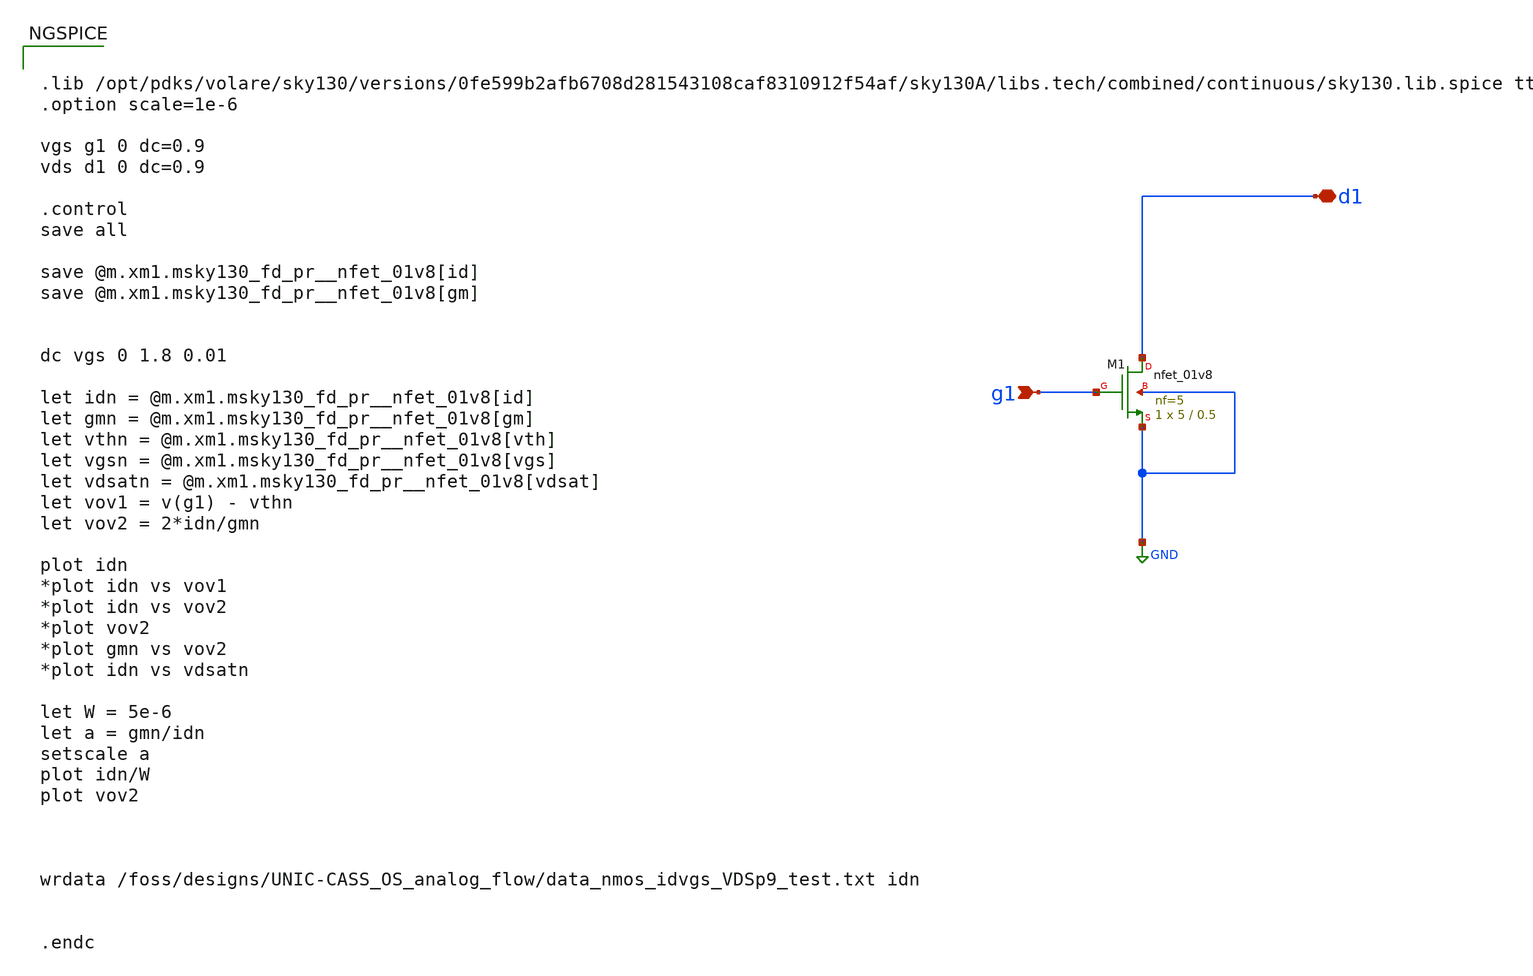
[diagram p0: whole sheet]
** sch_path: sky130_nmos_charac_noLVT.sch
**.subckt sky130_nmos_charac_noLVT g1 d1
*.ipin g1
*.iopin d1
XM1 d1 g1 GND GND sky130_fd_pr__nfet_01v8 L=0.5 W=5 nf=5 ad='int((nf+1)/2) * W/nf * 0.29' as='int((nf+2)/2) * W/nf * 0.29'
+ pd='2*int((nf+1)/2) * (W/nf + 0.29)' ps='2*int((nf+2)/2) * (W/nf + 0.29)' nrd='0.29 / W' nrs='0.29 / W'
+ sa=0 sb=0 sd=0 mult=1 m=1
**** begin user architecture code


.lib /opt/pdks/volare/sky130/versions/0fe599b2afb6708d281543108caf8310912f54af/sky130A/libs.tech/combined/continuous/sky130.lib.spice tt
.option scale=1e-6

vgs g1 0 dc=0.9
vds d1 0 dc=0.9

.control
save all

save @m.xm1.msky130_fd_pr__nfet_01v8[id]
save @m.xm1.msky130_fd_pr__nfet_01v8[gm]


dc vgs 0 1.8 0.01

let idn = @m.xm1.msky130_fd_pr__nfet_01v8[id]
let gmn = @m.xm1.msky130_fd_pr__nfet_01v8[gm]
let vthn = @m.xm1.msky130_fd_pr__nfet_01v8[vth]
let vgsn = @m.xm1.msky130_fd_pr__nfet_01v8[vgs]
let vdsatn = @m.xm1.msky130_fd_pr__nfet_01v8[vdsat]
let vov1 = v(g1) - vthn
let vov2 = 2*idn/gmn

plot idn
*plot idn vs vov1
*plot idn vs vov2
*plot vov2
*plot gmn vs vov2
*plot idn vs vdsatn

let W = 5e-6
let a = gmn/idn
setscale a
plot idn/W
plot vov2



wrdata /foss/designs/UNIC-CASS_OS_analog_flow/data_nmos_idvgs_VDSp9_test.txt idn


.endc


**** end user architecture code
**.ends
.GLOBAL GND
.end
